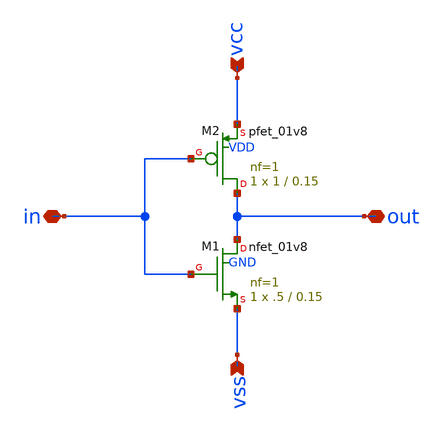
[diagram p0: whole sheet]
** sch_path: pll/ring_vco_lib/QRO_cell/xschem/FF_cell.sch
**.subckt FF_cell vss vcc out in
*.ipin vss
*.ipin vcc
*.iopin out
*.iopin in
XM1 out in vss GND sky130_fd_pr__nfet_01v8 L=0.15 W=.5 nf=1 ad='int((nf+1)/2) * W/nf * 0.29' as='int((nf+2)/2) * W/nf * 0.29'
+ pd='2*int((nf+1)/2) * (W/nf + 0.29)' ps='2*int((nf+2)/2) * (W/nf + 0.29)' nrd='0.29 / W' nrs='0.29 / W'
+ sa=0 sb=0 sd=0 mult=1 m=1
XM2 out in vcc VDD sky130_fd_pr__pfet_01v8 L=0.15 W=1 nf=1 ad='int((nf+1)/2) * W/nf * 0.29' as='int((nf+2)/2) * W/nf * 0.29'
+ pd='2*int((nf+1)/2) * (W/nf + 0.29)' ps='2*int((nf+2)/2) * (W/nf + 0.29)' nrd='0.29 / W' nrs='0.29 / W'
+ sa=0 sb=0 sd=0 mult=1 m=1
**.ends
.end
